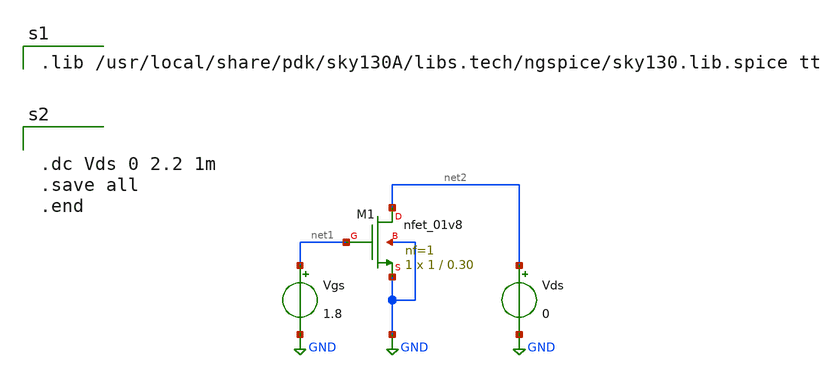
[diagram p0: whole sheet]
** sch_path: xschem files/nmos_char_1v8.sch
**.subckt nmos_char_1v8
XM1 net2 net1 GND GND sky130_fd_pr__nfet_01v8 L=0.30 W=1 nf=1 ad='int((nf+1)/2) * W/nf * 0.29' as='int((nf+2)/2) * W/nf * 0.29'
+ pd='2*int((nf+1)/2) * (W/nf + 0.29)' ps='2*int((nf+2)/2) * (W/nf + 0.29)' nrd='0.29 / W' nrs='0.29 / W'
+ sa=0 sb=0 sd=0 mult=1 m=1
Vgs net1 GND 1.8
Vds net2 GND 0
**** begin user architecture code

.lib /usr/local/share/pdk/sky130A/libs.tech/ngspice/sky130.lib.spice tt



.dc Vds 0 2.2 1m
.save all
.end


**** end user architecture code
**.ends
.GLOBAL GND
.end
